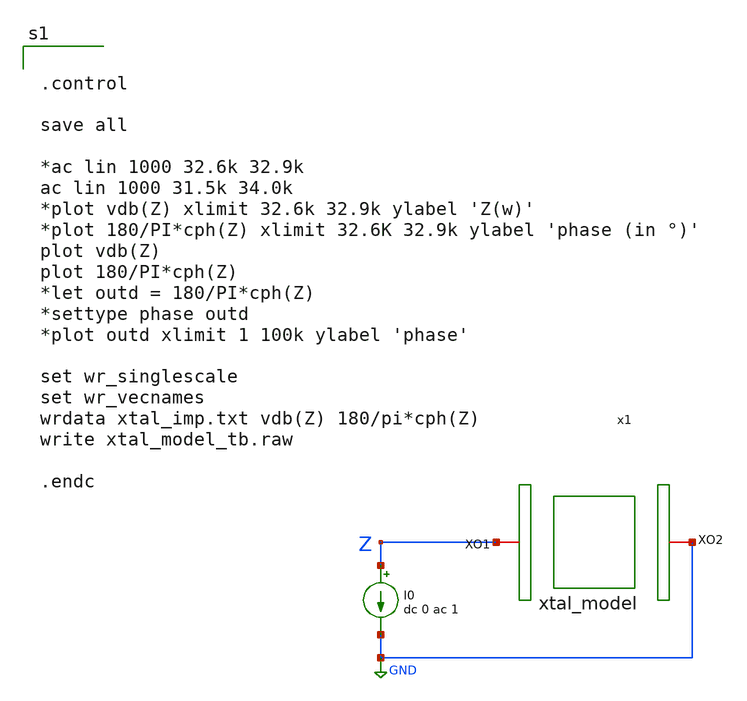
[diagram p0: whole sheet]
** sch_path: xtal_model_tb.sch
**.subckt xtal_model_tb
x1 Z GND xtal_model
I0 Z GND dc 0 ac 1
**** begin user architecture code


.control

save all

*ac lin 1000 32.6k 32.9k
ac lin 1000 31.5k 34.0k
*plot vdb(Z) xlimit 32.6k 32.9k ylabel 'Z(w)'
*plot 180/PI*cph(Z) xlimit 32.6K 32.9k ylabel 'phase (in °)'
plot vdb(Z)
plot 180/PI*cph(Z)
*let outd = 180/PI*cph(Z)
*settype phase outd
*plot outd xlimit 1 100k ylabel 'phase'

set wr_singlescale
set wr_vecnames
wrdata xtal_imp.txt vdb(Z) 180/pi*cph(Z)
write xtal_model_tb.raw

.endc


**** end user architecture code
**.ends

* expanding   symbol:  xtal_model.sym # of pins=2
** sym_path: xtal_model.sym
** sch_path: xtal_model.sch
.subckt xtal_model XO1 XO2
*.iopin XO2
*.iopin XO1
R1 XO1 net1 1k m=1
Cm net1 net2 1p m=1
C0 XO1 XO2 1p m=1
Lm net2 XO2 1n m=1
.ends

.GLOBAL GND
.end
